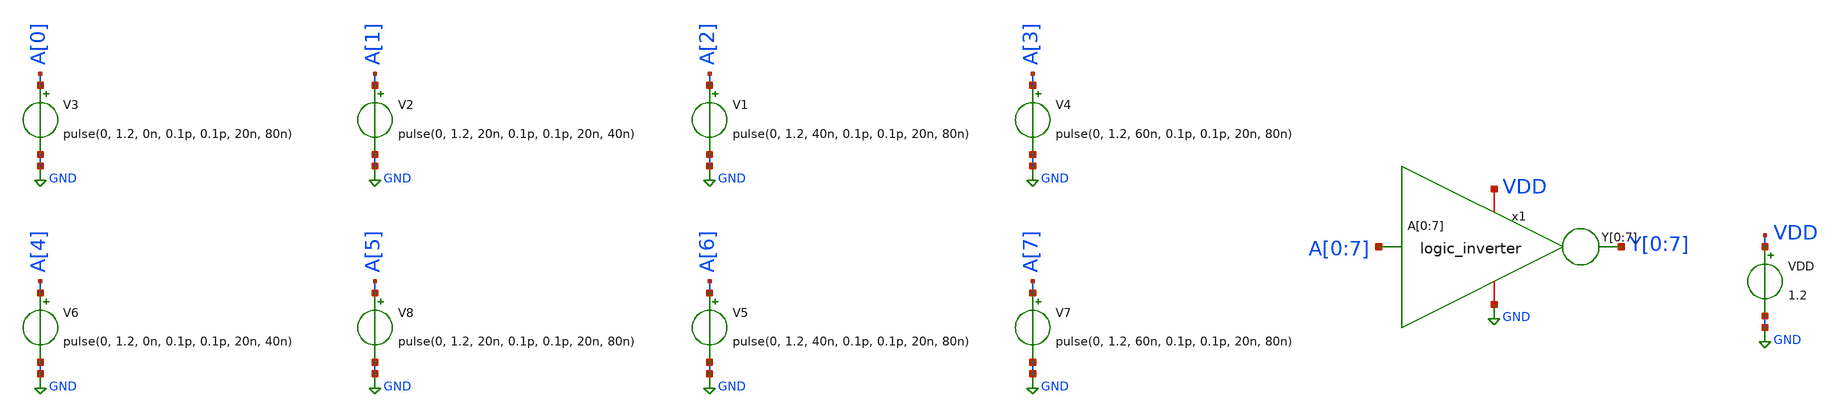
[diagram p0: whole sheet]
** sch_path: design/ALU/logic_inverter_tb.sch
**.subckt logic_inverter_tb
VDD VDD GND 1.2
V1 A[2] GND pulse(0, 1.2, 40n, 0.1p, 0.1p, 20n, 80n)
V3 A[0] GND pulse(0, 1.2, 0n, 0.1p, 0.1p, 20n, 80n)
V4 A[3] GND pulse(0, 1.2, 60n, 0.1p, 0.1p, 20n, 80n)
V2 A[1] GND pulse(0, 1.2, 20n, 0.1p, 0.1p, 20n, 40n)
V5 A[6] GND pulse(0, 1.2, 40n, 0.1p, 0.1p, 20n, 80n)
V6 A[4] GND pulse(0, 1.2, 0n, 0.1p, 0.1p, 20n, 40n)
V7 A[7] GND pulse(0, 1.2, 60n, 0.1p, 0.1p, 20n, 80n)
V8 A[5] GND pulse(0, 1.2, 20n, 0.1p, 0.1p, 20n, 80n)
x1 A[0] A[1] A[2] A[3] A[4] A[5] A[6] A[7] Y[0] Y[1] Y[2] Y[3] Y[4] Y[5] Y[6] Y[7] GND VDD
+ logic_inverter
**** begin user architecture code

** opencircuitdesign pdks install
.lib $::SKYWATER_MODELS/sky130.lib.spice tt_mm



.control
save all

set color0 = white
tran 1p 80n
plot "a[0]" "a[1]"+2 "a[2]"+4 "a[3]"+6 "a[4]"+8 "a[5]"+10 "a[6]"+12 "a[7]"+14
plot "y[0]" "y[1]"+2 "y[2]"+4 "y[3]"+6 "y[4]"+8 "y[5]"+10 "y[6]"+12 "y[7]"+14
.endc

**** end user architecture code
**.ends
.GLOBAL GND
.end
